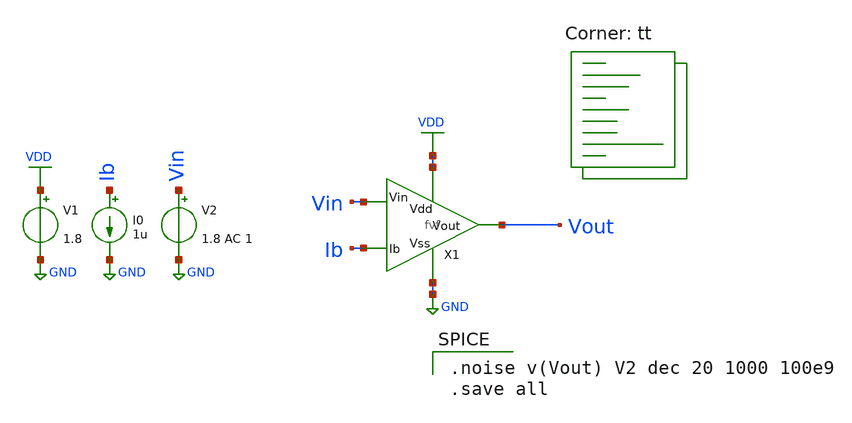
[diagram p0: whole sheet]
** sch_path: xschem/fvf_tb_noise.sch
**.subckt fvf_tb_noise
V1 VDD GND 1.8
I0 Ib GND 1u
X1 VDD GND Vin Vout Ib fvf
V2 Vin GND 1.8 AC 1
**** begin user architecture code
.lib $::SKYWATER_MODELS/sky130.lib.spice tt

.noise v(Vout) V2 dec 20 1000 100e9
.save all

**** end user architecture code
**.ends

* expanding   symbol:  /foss/designs/fvf-chipathon-2024/xschem/fvf.sym # of pins=5
** sym_path: xschem/fvf.sym
** sch_path: xschem/fvf.sch
.subckt fvf Vdd Vss Vin Vout Ib
*.ipin Vin
*.ipin Ib
*.opin Vout
*.iopin Vdd
*.iopin Vss
XM1 net1 Vin Vout GND sky130_fd_pr__nfet_01v8 L=1 W=15 nf=1 ad='int((nf+1)/2) * W/nf * 0.29' as='int((nf+2)/2) * W/nf * 0.29'
+ pd='2*int((nf+1)/2) * (W/nf + 0.29)' ps='2*int((nf+2)/2) * (W/nf + 0.29)' nrd='0.29 / W' nrs='0.29 / W'
+ sa=0 sb=0 sd=0 mult=1 m=1
XM2 Vout net1 Vss GND sky130_fd_pr__nfet_01v8 L=1 W=15 nf=1 ad='int((nf+1)/2) * W/nf * 0.29' as='int((nf+2)/2) * W/nf * 0.29'
+ pd='2*int((nf+1)/2) * (W/nf + 0.29)' ps='2*int((nf+2)/2) * (W/nf + 0.29)' nrd='0.29 / W' nrs='0.29 / W'
+ sa=0 sb=0 sd=0 mult=1 m=1
XM3 Ib Ib Vdd VDD sky130_fd_pr__pfet_01v8_lvt L=1 W=2 nf=1 ad='int((nf+1)/2) * W/nf * 0.29' as='int((nf+2)/2) * W/nf * 0.29'
+ pd='2*int((nf+1)/2) * (W/nf + 0.29)' ps='2*int((nf+2)/2) * (W/nf + 0.29)' nrd='0.29 / W' nrs='0.29 / W'
+ sa=0 sb=0 sd=0 mult=1 m=1
XM4 net1 Ib Vdd VDD sky130_fd_pr__pfet_01v8_lvt L=1 W=2 nf=1 ad='int((nf+1)/2) * W/nf * 0.29' as='int((nf+2)/2) * W/nf * 0.29'
+ pd='2*int((nf+1)/2) * (W/nf + 0.29)' ps='2*int((nf+2)/2) * (W/nf + 0.29)' nrd='0.29 / W' nrs='0.29 / W'
+ sa=0 sb=0 sd=0 mult=1 m=1
.ends

.GLOBAL VDD
.GLOBAL GND
.end
